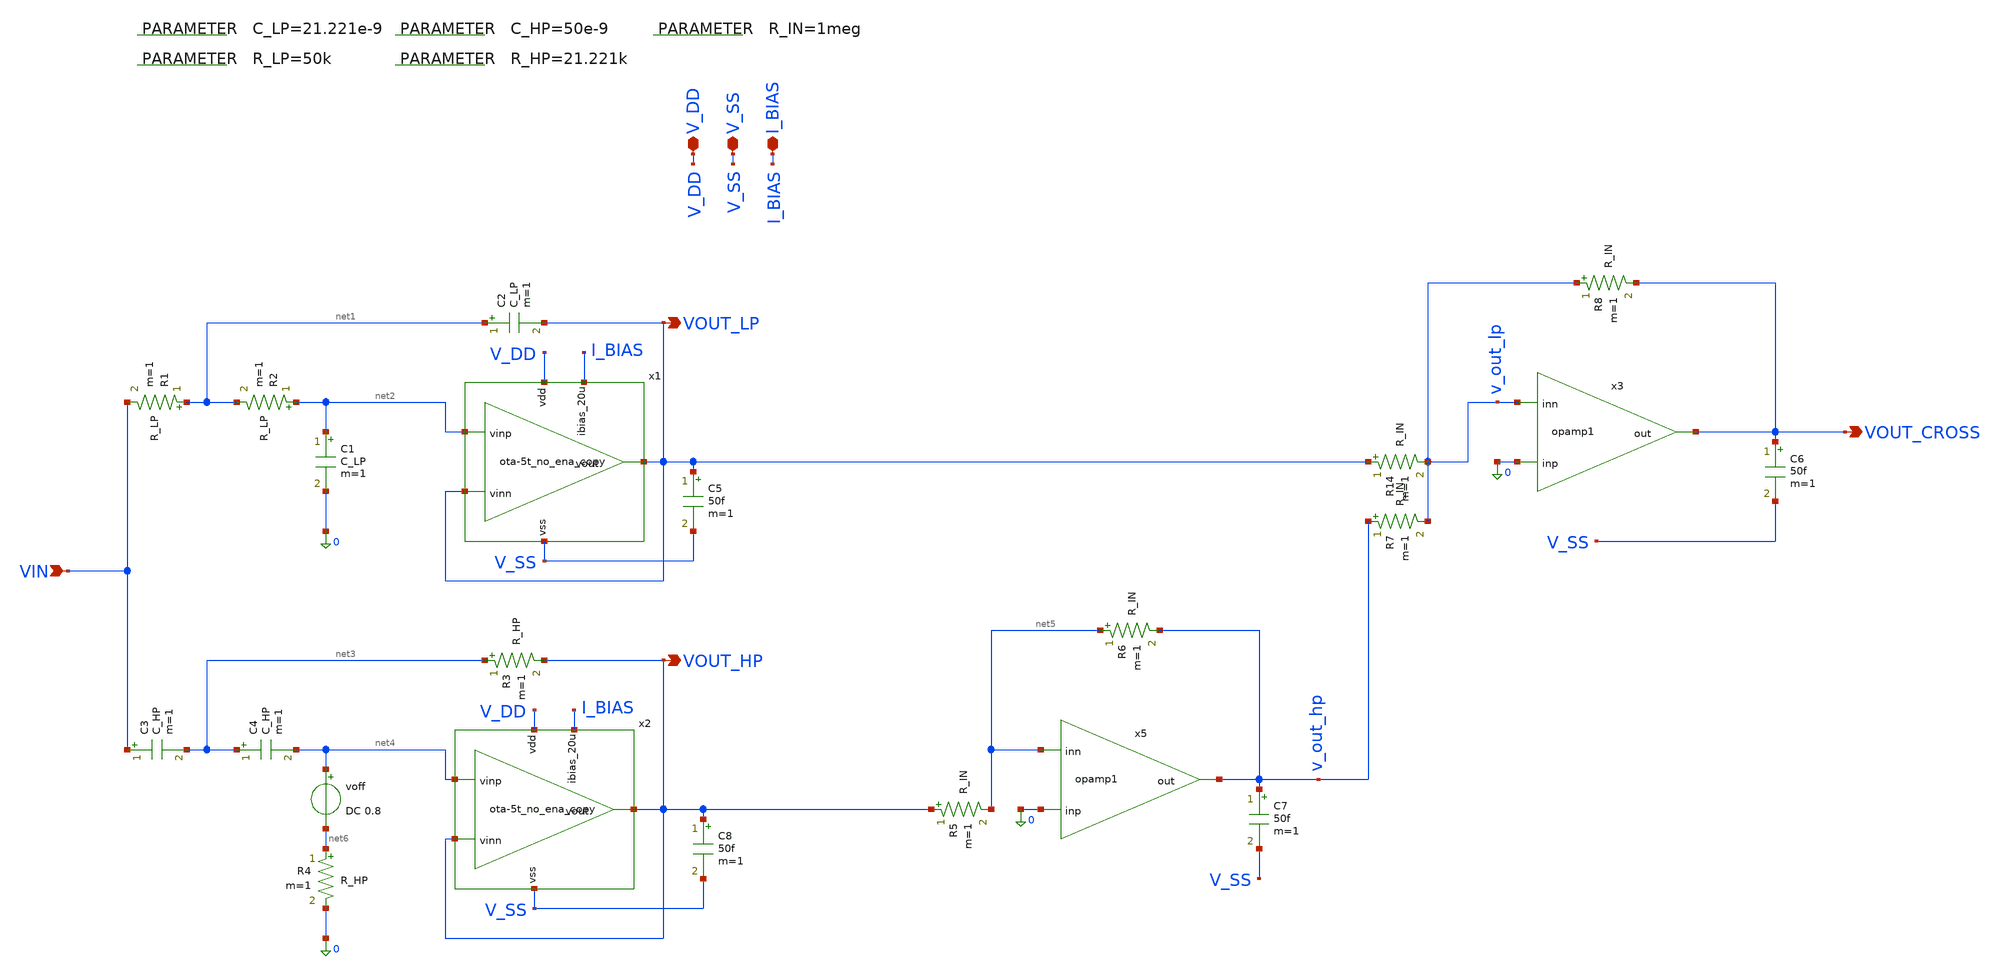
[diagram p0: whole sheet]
** sch_path: 004_Real_Circuits/003_version_second_output_stage/linkwtz_riley_crossover_pretl_OTA.sch
**.subckt linkwtz_riley_crossover_pretl_OTA VOUT_LP VIN V_DD VOUT_HP V_SS I_BIAS VOUT_CROSS
*.opin VOUT_LP
*.ipin VIN
*.iopin V_DD
*.opin VOUT_HP
*.iopin V_SS
*.iopin I_BIAS
*.opin VOUT_CROSS
R1 net1 VIN R_LP m=1
.param R_IN=1meg
R2 net2 net1 R_LP m=1
C1 net2 0 C_LP m=1
C2 net1 VOUT_LP C_LP m=1
C3 VIN net3 C_HP m=1
C4 net3 net4 C_HP m=1
R3 net3 VOUT_HP R_HP m=1
R4 net6 0 R_HP m=1
R5 VOUT_HP net5 R_IN m=1
R6 net5 v_out_hp R_IN m=1
R14 VOUT_LP v_out_lp R_IN m=1
R7 v_out_hp v_out_lp R_IN m=1
R8 v_out_lp VOUT_CROSS R_IN m=1
x1 V_DD VOUT_LP net2 VOUT_LP I_BIAS V_SS ota-5t_no_ena_copy
x2 V_DD VOUT_HP net4 VOUT_HP I_BIAS V_SS ota-5t_no_ena_copy
.param C_LP=21.221e-9
.param R_LP=50k
.param C_HP=50e-9
.param R_HP=21.221k
C5 VOUT_LP V_SS 50f m=1
C6 VOUT_CROSS V_SS 50f m=1
C7 v_out_hp V_SS 50f m=1
C8 VOUT_HP V_SS 50f m=1
voff net4 net6 DC 0.8
x5 0 net5 v_out_hp opamp1
x3 0 v_out_lp VOUT_CROSS opamp1
**.ends

* expanding   symbol:  004_Real_Circuits/003_version_second_output_stage/ota-5t_no_ena_copy.sym # of
*+ pins=6
** sym_path: 004_Real_Circuits/003_version_second_output_stage/ota-5t_no_ena_copy.sym
** sch_path: 004_Real_Circuits/003_version_second_output_stage/ota-5t_no_ena_copy.sch
.subckt ota-5t_no_ena_copy vdd vout vinp vinn ibias_20u vss
*.opin vout
*.iopin vdd
*.ipin vinp
*.ipin vinn
*.ipin ibias_20u
*.iopin vss
XM5 tail ibias_20u vss vss sg13_lv_nmos w=1.5u l=5u ng=1 m=1 mm_ok=1
XM4 net1 gate_p vdd vdd sg13_lv_pmos w=3.5u l=5u ng=1 m=1 mm_ok=1
XM1 gate_p vinn tail vss sg13_lv_nmos w=2u l=5u ng=1 m=1 mm_ok=1
XM2 net1 vinp tail vss sg13_lv_nmos w=2u l=5u ng=1 m=1 mm_ok=1
XM3 gate_p gate_p vdd vdd sg13_lv_pmos w=3.5u l=5u ng=1 m=1 mm_ok=1
XM6 ibias_20u ibias_20u vss vss sg13_lv_nmos w=10u l=5u ng=5 m=1 mm_ok=1
XM7 vout net1 vdd vdd sg13_lv_pmos w=8.5u l=5u ng=1 m=1 mm_ok=1
XM8 vout ibias_20u vss vss sg13_lv_nmos w=0.75u l=5u ng=1 m=1 mm_ok=1
C2 net2 vout 795f m=1
R1 net1 net2 59k m=1
.ends


* expanding   symbol:  001_provided_files/2_Idealized_circuits/opamp1.sym # of pins=3
** sym_path: 001_provided_files/2_Idealized_circuits/opamp1.sym
** sch_path: 001_provided_files/2_Idealized_circuits/opamp1.sch
.subckt opamp1 inp inn out
*.ipin inp
*.ipin inn
*.opin out
Rin inp inn 10MEG m=1
Rout net2 out 10 m=1
Cp net1 GND 1.59u m=1
Rp GND net1 1k m=1
Ebuf net2 GND net1 GND 1
G1 net1 GND inp inn 1
.ends

.GLOBAL GND
.end
